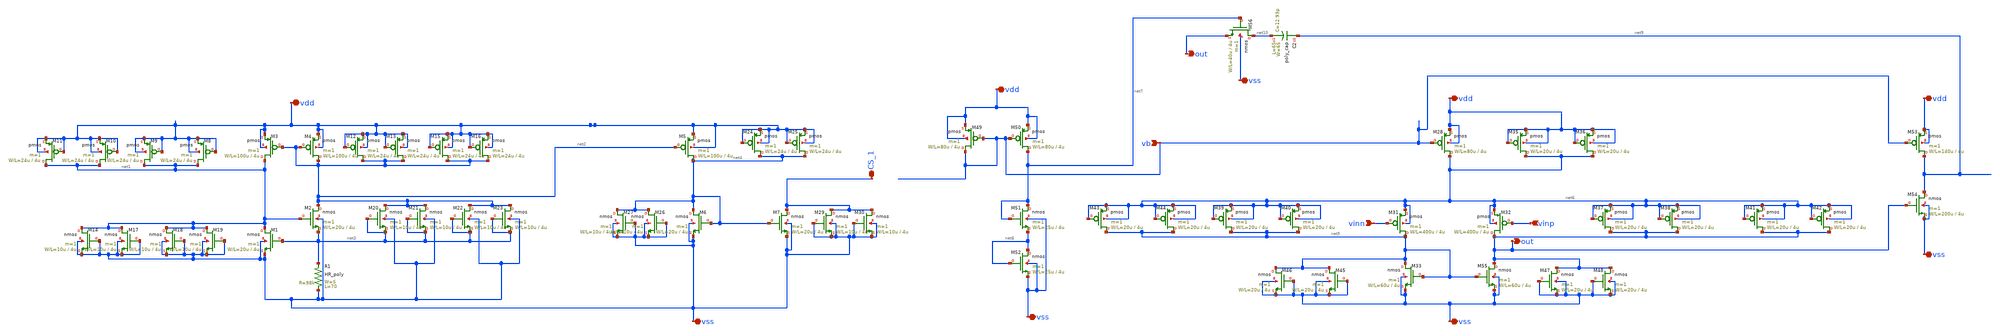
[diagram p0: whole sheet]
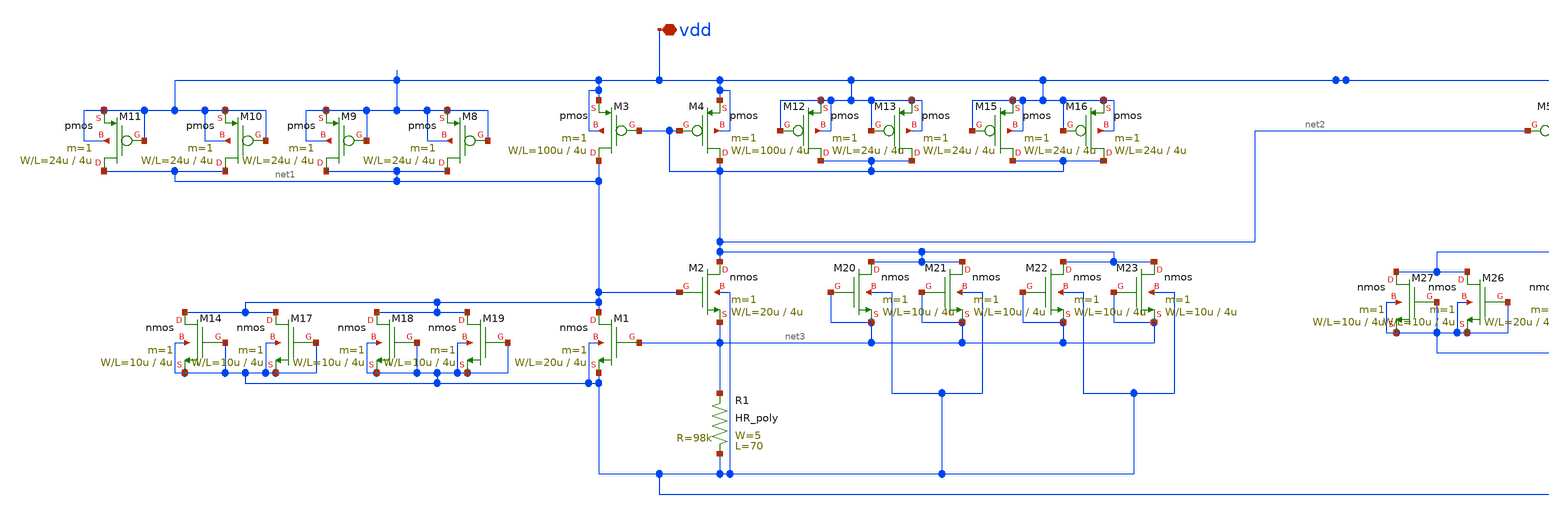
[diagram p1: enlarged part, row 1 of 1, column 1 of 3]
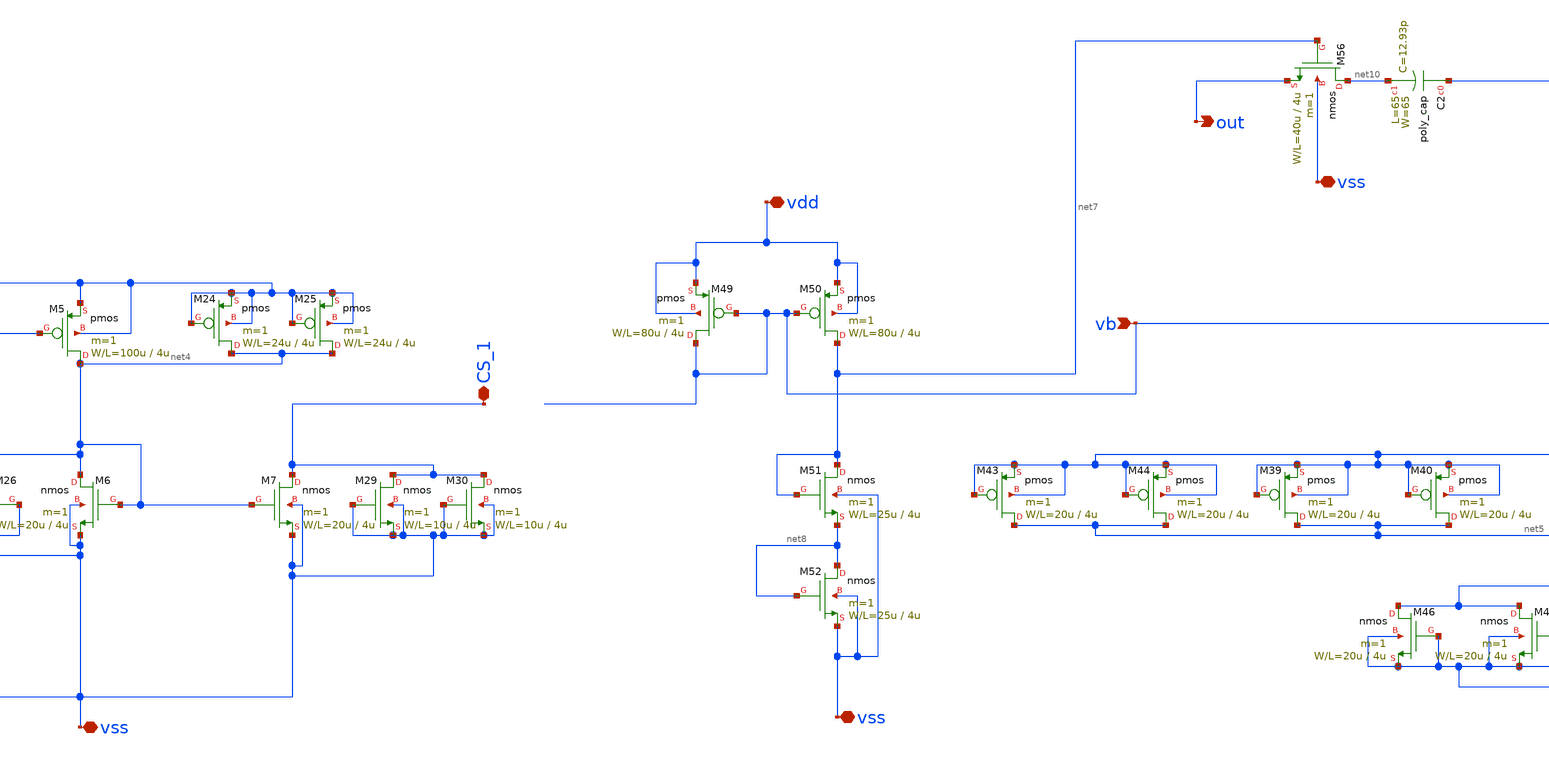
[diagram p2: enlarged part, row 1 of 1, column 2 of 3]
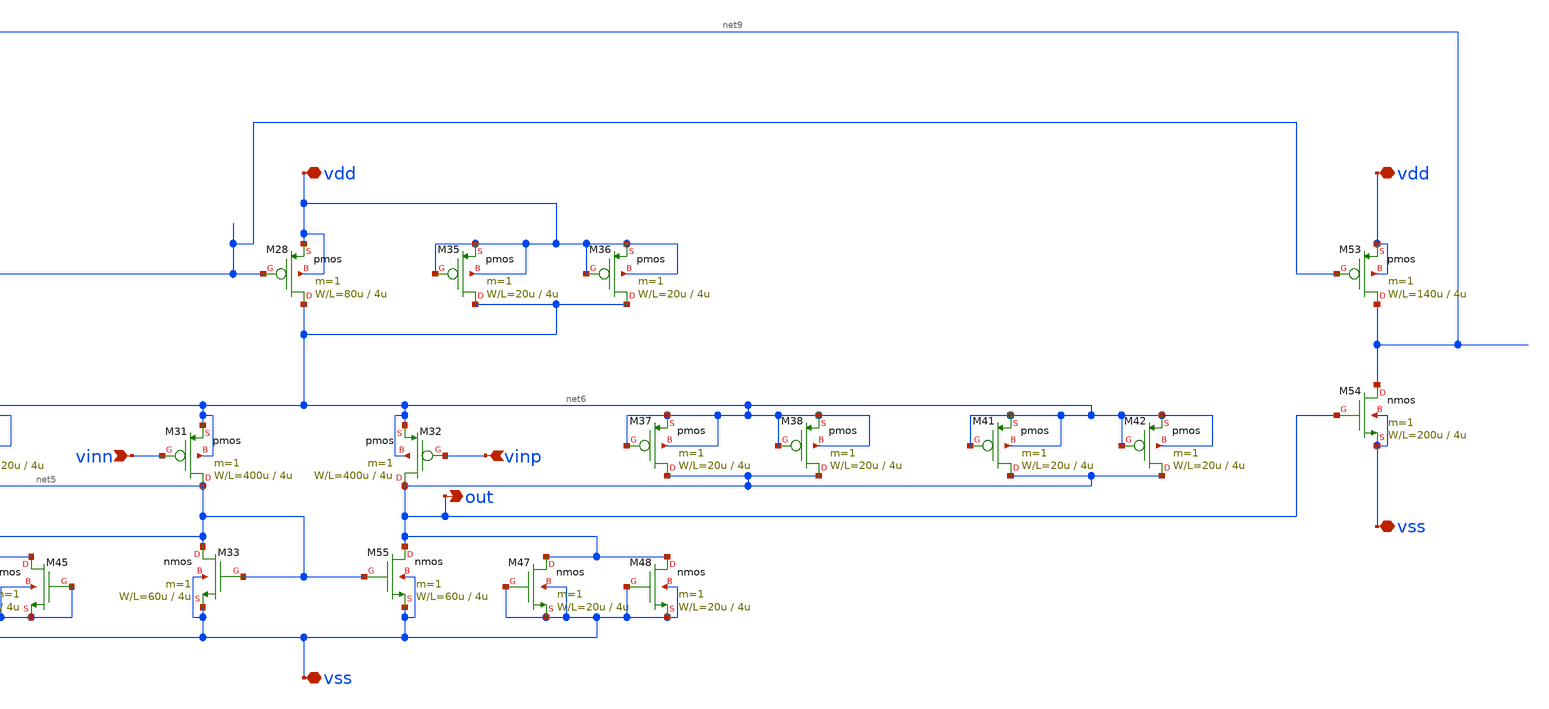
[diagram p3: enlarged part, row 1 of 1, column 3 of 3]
** sch_path: member_project/GroupWork/Team_ichiken/opamp_ichiken_v3.sch
**.subckt opamp_ichiken_v3 vdd vss vinn vinp vb out vdd vss vss vdd vss vdd vss out CS_1
*.iopin vdd
*.iopin vss
*.ipin vinn
*.ipin vinp
*.ipin vb
*.opin out
*.iopin vdd
*.iopin vss
*.iopin vss
*.iopin vdd
*.iopin vss
*.iopin vdd
*.iopin vss
*.opin out
*.iopin CS_1
M4 net2 net2 vdd vdd pmos L=4u W=100u m=1
M3 net1 net2 vdd vdd pmos L=4u W=100u m=1
M2 net2 net1 net3 vss nmos L=4u W=20u m=1
M1 net1 net3 vss vss nmos L=4u W=20u m=1
M5 net4 net2 vdd vdd pmos L=4u W=100u m=1
M6 net4 net4 vss vss nmos L=4u W=20u m=1
M7 CS_1 net4 vss vss nmos L=4u W=20u m=1
M8 net1 vdd vdd vdd pmos L=4u W=24u m=1
M9 net1 vdd vdd vdd pmos L=4u W=24u m=1
M10 net1 vdd vdd vdd pmos L=4u W=24u m=1
M11 net1 vdd vdd vdd pmos L=4u W=24u m=1
M13 net2 vdd vdd vdd pmos L=4u W=24u m=1
M12 net2 vdd vdd vdd pmos L=4u W=24u m=1
M15 net2 vdd vdd vdd pmos L=4u W=24u m=1
M16 net2 vdd vdd vdd pmos L=4u W=24u m=1
M24 net4 vdd vdd vdd pmos L=4u W=24u m=1
M25 net4 vdd vdd vdd pmos L=4u W=24u m=1
M26 net4 vss vss vss nmos L=4u W=10u m=1
M27 net4 vss vss vss nmos L=4u W=10u m=1
M29 CS_1 vss vss vss nmos L=4u W=10u m=1
M30 CS_1 vss vss vss nmos L=4u W=10u m=1
M28 net6 vb vdd vdd pmos L=4u W=80u m=1
M31 net5 vinn net6 net6 pmos L=4u W=400u m=1
M32 out vinp net6 net6 pmos L=4u W=400u m=1
M33 net5 net5 vss vss nmos L=4u W=60u m=1
M35 net6 vdd vdd vdd pmos L=4u W=20u m=1
M36 net6 vdd vdd vdd pmos L=4u W=20u m=1
M37 out net6 net6 net6 pmos L=4u W=20u m=1
M38 out net6 net6 net6 pmos L=4u W=20u m=1
M39 net5 net6 net6 net6 pmos L=4u W=20u m=1
M40 net5 net6 net6 net6 pmos L=4u W=20u m=1
M41 out net6 net6 net6 pmos L=4u W=20u m=1
M42 out net6 net6 net6 pmos L=4u W=20u m=1
M43 net5 net6 net6 net6 pmos L=4u W=20u m=1
M44 net5 net6 net6 net6 pmos L=4u W=20u m=1
M45 net5 vss vss vss nmos L=4u W=20u m=1
M46 net5 vss vss vss nmos L=4u W=20u m=1
M47 out vss vss vss nmos L=4u W=20u m=1
M48 out vss vss vss nmos L=4u W=20u m=1
M49 vb vb vdd vdd pmos L=4u W=80u m=1
M51 net7 net7 net8 vss nmos L=4u W=25u m=1
M52 net8 net8 vss vss nmos L=4u W=25u m=1
M53 net9 vb vdd vdd pmos L=4u W=140u m=1
M54 net9 out vss vss nmos L=4u W=200u m=1
M55 out net5 vss vss nmos L=4u W=60u m=1
M56 net10 net7 out vss nmos L=4u W=40u m=1
R1 vss net3 HR_poly W=5 L=70
M20 net2 net3 net3 vss nmos L=4u W=10u m=1
M21 net2 net3 net3 vss nmos L=4u W=10u m=1
M22 net2 net3 net3 vss nmos L=4u W=10u m=1
M23 net2 net3 net3 vss nmos L=4u W=10u m=1
M14 net1 vss vss vss nmos L=4u W=10u m=1
M17 net1 vss vss vss nmos L=4u W=10u m=1
M18 net1 vss vss vss nmos L=4u W=10u m=1
M19 net1 vss vss vss nmos L=4u W=10u m=1
M50 net7 vb vdd vdd pmos L=4u W=80u m=1
C2 net9 net10 poly_cap W=65 L=65
**.ends
.end
